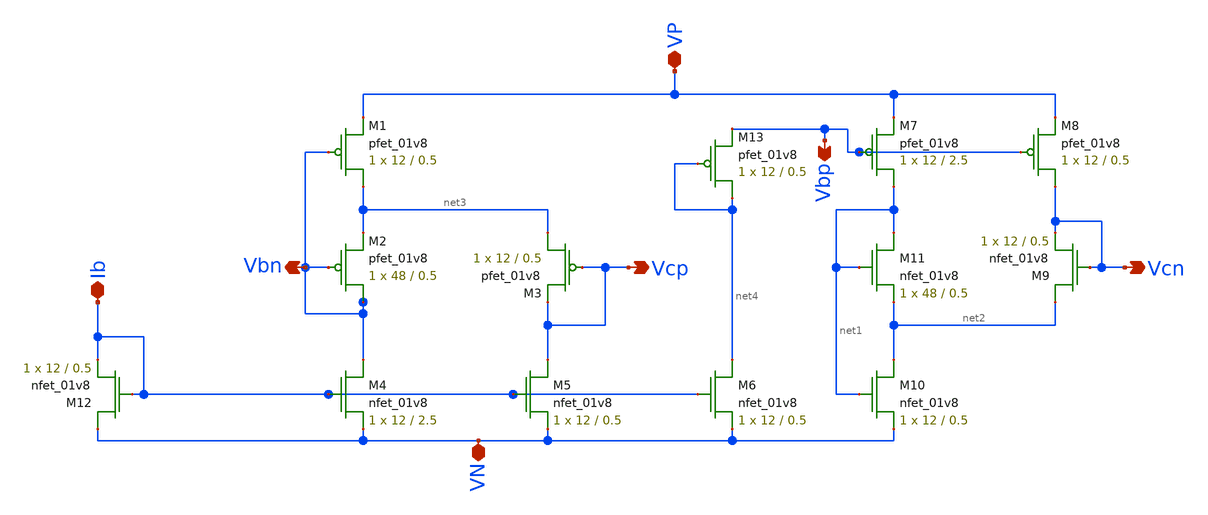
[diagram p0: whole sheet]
** sch_path: mp3/schematic/bias.sch
**.subckt bias VP VN Vcp Vcn Vbp Ib Vbn
*.iopin VP
*.iopin VN
*.opin Vcp
*.opin Vcn
*.opin Vbp
*.iopin Ib
*.opin Vbn
XM1 net3 Vbn VP VDD sky130_fd_pr__pfet_01v8 L=0.5 W=12 nf=1 ad='int((nf+1)/2) * W/nf * 0.29' as='int((nf+2)/2) * W/nf * 0.29'
+ pd='2*int((nf+1)/2) * (W/nf + 0.29)' ps='2*int((nf+2)/2) * (W/nf + 0.29)' nrd='0.29 / W' nrs='0.29 / W'
+ sa=0 sb=0 sd=0 mult=1 m=1
XM2 Vbn Vbn net3 VDD sky130_fd_pr__pfet_01v8 L=0.5 W=48 nf=1 ad='int((nf+1)/2) * W/nf * 0.29' as='int((nf+2)/2) * W/nf * 0.29'
+ pd='2*int((nf+1)/2) * (W/nf + 0.29)' ps='2*int((nf+2)/2) * (W/nf + 0.29)' nrd='0.29 / W' nrs='0.29 / W'
+ sa=0 sb=0 sd=0 mult=1 m=1
XM3 net3 Vcp Vcp VDD sky130_fd_pr__pfet_01v8 L=0.5 W=12 nf=1 ad='int((nf+1)/2) * W/nf * 0.29' as='int((nf+2)/2) * W/nf * 0.29'
+ pd='2*int((nf+1)/2) * (W/nf + 0.29)' ps='2*int((nf+2)/2) * (W/nf + 0.29)' nrd='0.29 / W' nrs='0.29 / W'
+ sa=0 sb=0 sd=0 mult=1 m=1
XM4 Vbn Ib VN GND sky130_fd_pr__nfet_01v8 L=2.5 W=12 nf=1 ad='int((nf+1)/2) * W/nf * 0.29' as='int((nf+2)/2) * W/nf * 0.29'
+ pd='2*int((nf+1)/2) * (W/nf + 0.29)' ps='2*int((nf+2)/2) * (W/nf + 0.29)' nrd='0.29 / W' nrs='0.29 / W'
+ sa=0 sb=0 sd=0 mult=1 m=1
XM5 Vcp Ib VN GND sky130_fd_pr__nfet_01v8 L=0.5 W=12 nf=1 ad='int((nf+1)/2) * W/nf * 0.29' as='int((nf+2)/2) * W/nf * 0.29'
+ pd='2*int((nf+1)/2) * (W/nf + 0.29)' ps='2*int((nf+2)/2) * (W/nf + 0.29)' nrd='0.29 / W' nrs='0.29 / W'
+ sa=0 sb=0 sd=0 mult=1 m=1
XM6 net4 Ib VN GND sky130_fd_pr__nfet_01v8 L=0.5 W=12 nf=1 ad='int((nf+1)/2) * W/nf * 0.29' as='int((nf+2)/2) * W/nf * 0.29'
+ pd='2*int((nf+1)/2) * (W/nf + 0.29)' ps='2*int((nf+2)/2) * (W/nf + 0.29)' nrd='0.29 / W' nrs='0.29 / W'
+ sa=0 sb=0 sd=0 mult=1 m=1
XM7 net1 Vbp VP VDD sky130_fd_pr__pfet_01v8 L=2.5 W=12 nf=1 ad='int((nf+1)/2) * W/nf * 0.29' as='int((nf+2)/2) * W/nf * 0.29'
+ pd='2*int((nf+1)/2) * (W/nf + 0.29)' ps='2*int((nf+2)/2) * (W/nf + 0.29)' nrd='0.29 / W' nrs='0.29 / W'
+ sa=0 sb=0 sd=0 mult=1 m=1
XM8 Vcn Vbp VP VDD sky130_fd_pr__pfet_01v8 L=0.5 W=12 nf=1 ad='int((nf+1)/2) * W/nf * 0.29' as='int((nf+2)/2) * W/nf * 0.29'
+ pd='2*int((nf+1)/2) * (W/nf + 0.29)' ps='2*int((nf+2)/2) * (W/nf + 0.29)' nrd='0.29 / W' nrs='0.29 / W'
+ sa=0 sb=0 sd=0 mult=1 m=1
XM9 net2 Vcn Vcn GND sky130_fd_pr__nfet_01v8 L=0.5 W=12 nf=1 ad='int((nf+1)/2) * W/nf * 0.29' as='int((nf+2)/2) * W/nf * 0.29'
+ pd='2*int((nf+1)/2) * (W/nf + 0.29)' ps='2*int((nf+2)/2) * (W/nf + 0.29)' nrd='0.29 / W' nrs='0.29 / W'
+ sa=0 sb=0 sd=0 mult=1 m=1
XM10 net2 net1 VN GND sky130_fd_pr__nfet_01v8 L=0.5 W=12 nf=1 ad='int((nf+1)/2) * W/nf * 0.29' as='int((nf+2)/2) * W/nf * 0.29'
+ pd='2*int((nf+1)/2) * (W/nf + 0.29)' ps='2*int((nf+2)/2) * (W/nf + 0.29)' nrd='0.29 / W' nrs='0.29 / W'
+ sa=0 sb=0 sd=0 mult=1 m=1
XM11 net1 net1 net2 GND sky130_fd_pr__nfet_01v8 L=0.5 W=48 nf=1 ad='int((nf+1)/2) * W/nf * 0.29' as='int((nf+2)/2) * W/nf * 0.29'
+ pd='2*int((nf+1)/2) * (W/nf + 0.29)' ps='2*int((nf+2)/2) * (W/nf + 0.29)' nrd='0.29 / W' nrs='0.29 / W'
+ sa=0 sb=0 sd=0 mult=1 m=1
XM12 VN Ib Ib GND sky130_fd_pr__nfet_01v8 L=0.5 W=12 nf=1 ad='int((nf+1)/2) * W/nf * 0.29' as='int((nf+2)/2) * W/nf * 0.29'
+ pd='2*int((nf+1)/2) * (W/nf + 0.29)' ps='2*int((nf+2)/2) * (W/nf + 0.29)' nrd='0.29 / W' nrs='0.29 / W'
+ sa=0 sb=0 sd=0 mult=1 m=1
XM13 net4 net4 Vbp VDD sky130_fd_pr__pfet_01v8 L=0.5 W=12 nf=1 ad='int((nf+1)/2) * W/nf * 0.29' as='int((nf+2)/2) * W/nf * 0.29'
+ pd='2*int((nf+1)/2) * (W/nf + 0.29)' ps='2*int((nf+2)/2) * (W/nf + 0.29)' nrd='0.29 / W' nrs='0.29 / W'
+ sa=0 sb=0 sd=0 mult=1 m=1
**.ends
.end
